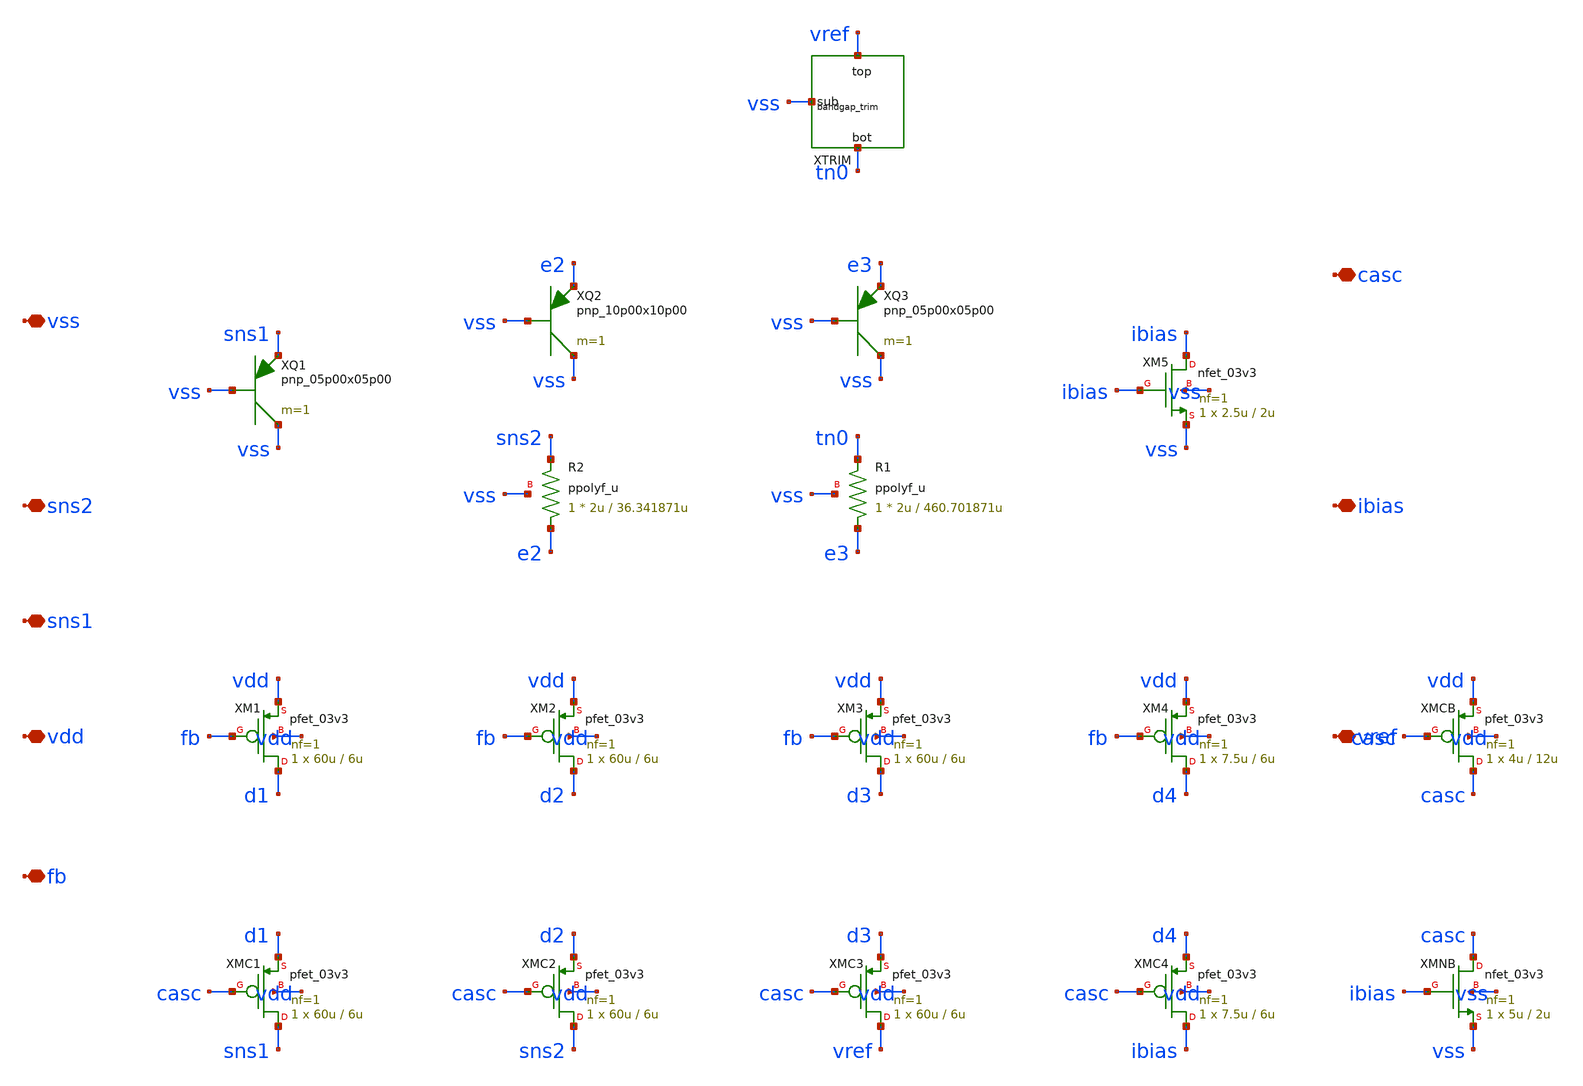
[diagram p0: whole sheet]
** sch_path: design/bandgap_core.sch
**.subckt bandgap_core vdd vss fb sns1 sns2 vref ibias casc
*.iopin vdd
*.iopin vss
*.iopin fb
*.iopin sns1
*.iopin sns2
*.iopin vref
*.iopin ibias
*.iopin casc
XM1 d1 fb vdd vdd pfet_03v3 L=6u W=60u nf=1 ad='int((nf+1)/2) * W/nf * 0.18u' as='int((nf+2)/2) * W/nf * 0.18u'
+ pd='2*int((nf+1)/2) * (W/nf + 0.18u)' ps='2*int((nf+2)/2) * (W/nf + 0.18u)' nrd='0.18u / W' nrs='0.18u / W'
+ sa=0 sb=0 sd=0 m=1
XMC1 sns1 casc d1 vdd pfet_03v3 L=6u W=60u nf=1 ad='int((nf+1)/2) * W/nf * 0.18u' as='int((nf+2)/2) * W/nf * 0.18u'
+ pd='2*int((nf+1)/2) * (W/nf + 0.18u)' ps='2*int((nf+2)/2) * (W/nf + 0.18u)' nrd='0.18u / W' nrs='0.18u / W'
+ sa=0 sb=0 sd=0 m=1
XQ1 vss vss sns1 pnp_05p00x05p00 m=1 par=1
XM2 d2 fb vdd vdd pfet_03v3 L=6u W=60u nf=1 ad='int((nf+1)/2) * W/nf * 0.18u' as='int((nf+2)/2) * W/nf * 0.18u'
+ pd='2*int((nf+1)/2) * (W/nf + 0.18u)' ps='2*int((nf+2)/2) * (W/nf + 0.18u)' nrd='0.18u / W' nrs='0.18u / W'
+ sa=0 sb=0 sd=0 m=1
XMC2 sns2 casc d2 vdd pfet_03v3 L=6u W=60u nf=1 ad='int((nf+1)/2) * W/nf * 0.18u' as='int((nf+2)/2) * W/nf * 0.18u'
+ pd='2*int((nf+1)/2) * (W/nf + 0.18u)' ps='2*int((nf+2)/2) * (W/nf + 0.18u)' nrd='0.18u / W' nrs='0.18u / W'
+ sa=0 sb=0 sd=0 m=1
XR2 e2 sns2 vss ppolyf_u r_width=2u r_length=36.341871u m=1
XQ2 vss vss e2 pnp_10p00x10p00 m=1
XM3 d3 fb vdd vdd pfet_03v3 L=6u W=60u nf=1 ad='int((nf+1)/2) * W/nf * 0.18u' as='int((nf+2)/2) * W/nf * 0.18u'
+ pd='2*int((nf+1)/2) * (W/nf + 0.18u)' ps='2*int((nf+2)/2) * (W/nf + 0.18u)' nrd='0.18u / W' nrs='0.18u / W'
+ sa=0 sb=0 sd=0 m=1
XMC3 vref casc d3 vdd pfet_03v3 L=6u W=60u nf=1 ad='int((nf+1)/2) * W/nf * 0.18u' as='int((nf+2)/2) * W/nf * 0.18u'
+ pd='2*int((nf+1)/2) * (W/nf + 0.18u)' ps='2*int((nf+2)/2) * (W/nf + 0.18u)' nrd='0.18u / W' nrs='0.18u / W'
+ sa=0 sb=0 sd=0 m=1
XR1 e3 tn0 vss ppolyf_u r_width=2u r_length=460.701871u m=1
XQ3 vss vss e3 pnp_05p00x05p00 m=1 par=1
XM4 d4 fb vdd vdd pfet_03v3 L=6u W=7.5u nf=1 ad='int((nf+1)/2) * W/nf * 0.18u' as='int((nf+2)/2) * W/nf * 0.18u'
+ pd='2*int((nf+1)/2) * (W/nf + 0.18u)' ps='2*int((nf+2)/2) * (W/nf + 0.18u)' nrd='0.18u / W' nrs='0.18u / W'
+ sa=0 sb=0 sd=0 m=1
XMC4 ibias casc d4 vdd pfet_03v3 L=6u W=7.5u nf=1 ad='int((nf+1)/2) * W/nf * 0.18u' as='int((nf+2)/2) * W/nf * 0.18u'
+ pd='2*int((nf+1)/2) * (W/nf + 0.18u)' ps='2*int((nf+2)/2) * (W/nf + 0.18u)' nrd='0.18u / W' nrs='0.18u / W'
+ sa=0 sb=0 sd=0 m=1
XM5 ibias ibias vss vss nfet_03v3 L=2u W=2.5u nf=1 ad='int((nf+1)/2) * W/nf * 0.18u' as='int((nf+2)/2) * W/nf * 0.18u'
+ pd='2*int((nf+1)/2) * (W/nf + 0.18u)' ps='2*int((nf+2)/2) * (W/nf + 0.18u)' nrd='0.18u / W' nrs='0.18u / W'
+ sa=0 sb=0 sd=0 m=1
XMCB casc casc vdd vdd pfet_03v3 L=12u W=4u nf=1 ad='int((nf+1)/2) * W/nf * 0.18u' as='int((nf+2)/2) * W/nf * 0.18u'
+ pd='2*int((nf+1)/2) * (W/nf + 0.18u)' ps='2*int((nf+2)/2) * (W/nf + 0.18u)' nrd='0.18u / W' nrs='0.18u / W'
+ sa=0 sb=0 sd=0 m=1
XMNB casc ibias vss vss nfet_03v3 L=2u W=5u nf=1 ad='int((nf+1)/2) * W/nf * 0.18u' as='int((nf+2)/2) * W/nf * 0.18u'
+ pd='2*int((nf+1)/2) * (W/nf + 0.18u)' ps='2*int((nf+2)/2) * (W/nf + 0.18u)' nrd='0.18u / W' nrs='0.18u / W'
+ sa=0 sb=0 sd=0 m=1
XXTRIM tn0 vref vss bandgap_trim
**.ends

* expanding   symbol:  bandgap_trim.sym # of pins=3
** sym_path: design/bandgap_trim.sym
** sch_path: design/bandgap_trim.sch
.subckt bandgap_trim bot top sub

*.iopin bot
*.iopin top
*.iopin sub
**** begin user architecture code

.param trim_code=32

**** end user architecture code
XRU0 bot tn1 sub ppolyf_u r_width=2u r_length=2.771871u m=1
RS0 tn1 bot {1e-3 + 1e12*(floor(trim_code/1)-2*floor(trim_code/2))} m=1
XRU1 tn1 u1_0 sub ppolyf_u r_width=2u r_length=2.771871u m=1
XRU2 u1_0 tn2 sub ppolyf_u r_width=2u r_length=2.771871u m=1
RS1 tn2 tn1 {1e-3 + 1e12*(floor(trim_code/2)-2*floor(trim_code/4))} m=1
XRU3 tn2 u2_0 sub ppolyf_u r_width=2u r_length=2.771871u m=1
XRU4 u2_0 u2_1 sub ppolyf_u r_width=2u r_length=2.771871u m=1
XRU5 u2_1 u2_2 sub ppolyf_u r_width=2u r_length=2.771871u m=1
XRU6 u2_2 tn3 sub ppolyf_u r_width=2u r_length=2.771871u m=1
RS2 tn3 tn2 {1e-3 + 1e12*(floor(trim_code/4)-2*floor(trim_code/8))} m=1
XRU7 tn3 u3_0 sub ppolyf_u r_width=2u r_length=2.771871u m=1
XRU8 u3_0 u3_1 sub ppolyf_u r_width=2u r_length=2.771871u m=1
XRU9 u3_1 u3_2 sub ppolyf_u r_width=2u r_length=2.771871u m=1
XRU10 u3_2 u3_3 sub ppolyf_u r_width=2u r_length=2.771871u m=1
XRU11 u3_3 u3_4 sub ppolyf_u r_width=2u r_length=2.771871u m=1
XRU12 u3_4 u3_5 sub ppolyf_u r_width=2u r_length=2.771871u m=1
XRU13 u3_5 u3_6 sub ppolyf_u r_width=2u r_length=2.771871u m=1
XRU14 u3_6 tn4 sub ppolyf_u r_width=2u r_length=2.771871u m=1
RS3 tn4 tn3 {1e-3 + 1e12*(floor(trim_code/8)-2*floor(trim_code/16))} m=1
XRU15 tn4 u4_0 sub ppolyf_u r_width=2u r_length=2.771871u m=1
XRU16 u4_0 u4_1 sub ppolyf_u r_width=2u r_length=2.771871u m=1
XRU17 u4_1 u4_2 sub ppolyf_u r_width=2u r_length=2.771871u m=1
XRU18 u4_2 u4_3 sub ppolyf_u r_width=2u r_length=2.771871u m=1
XRU19 u4_3 u4_4 sub ppolyf_u r_width=2u r_length=2.771871u m=1
XRU20 u4_4 u4_5 sub ppolyf_u r_width=2u r_length=2.771871u m=1
XRU21 u4_5 u4_6 sub ppolyf_u r_width=2u r_length=2.771871u m=1
XRU22 u4_6 u4_7 sub ppolyf_u r_width=2u r_length=2.771871u m=1
XRU23 u4_7 u4_8 sub ppolyf_u r_width=2u r_length=2.771871u m=1
XRU24 u4_8 u4_9 sub ppolyf_u r_width=2u r_length=2.771871u m=1
XRU25 u4_9 u4_10 sub ppolyf_u r_width=2u r_length=2.771871u m=1
XRU26 u4_10 u4_11 sub ppolyf_u r_width=2u r_length=2.771871u m=1
XRU27 u4_11 u4_12 sub ppolyf_u r_width=2u r_length=2.771871u m=1
XRU28 u4_12 u4_13 sub ppolyf_u r_width=2u r_length=2.771871u m=1
XRU29 u4_13 u4_14 sub ppolyf_u r_width=2u r_length=2.771871u m=1
XRU30 u4_14 tn5 sub ppolyf_u r_width=2u r_length=2.771871u m=1
RS4 tn5 tn4 {1e-3 + 1e12*(floor(trim_code/16)-2*floor(trim_code/32))} m=1
XRU31 tn5 u5_0 sub ppolyf_u r_width=2u r_length=2.771871u m=1
XRU32 u5_0 u5_1 sub ppolyf_u r_width=2u r_length=2.771871u m=1
XRU33 u5_1 u5_2 sub ppolyf_u r_width=2u r_length=2.771871u m=1
XRU34 u5_2 u5_3 sub ppolyf_u r_width=2u r_length=2.771871u m=1
XRU35 u5_3 u5_4 sub ppolyf_u r_width=2u r_length=2.771871u m=1
XRU36 u5_4 u5_5 sub ppolyf_u r_width=2u r_length=2.771871u m=1
XRU37 u5_5 u5_6 sub ppolyf_u r_width=2u r_length=2.771871u m=1
XRU38 u5_6 u5_7 sub ppolyf_u r_width=2u r_length=2.771871u m=1
XRU39 u5_7 u5_8 sub ppolyf_u r_width=2u r_length=2.771871u m=1
XRU40 u5_8 u5_9 sub ppolyf_u r_width=2u r_length=2.771871u m=1
XRU41 u5_9 u5_10 sub ppolyf_u r_width=2u r_length=2.771871u m=1
XRU42 u5_10 u5_11 sub ppolyf_u r_width=2u r_length=2.771871u m=1
XRU43 u5_11 u5_12 sub ppolyf_u r_width=2u r_length=2.771871u m=1
XRU44 u5_12 u5_13 sub ppolyf_u r_width=2u r_length=2.771871u m=1
XRU45 u5_13 u5_14 sub ppolyf_u r_width=2u r_length=2.771871u m=1
XRU46 u5_14 u5_15 sub ppolyf_u r_width=2u r_length=2.771871u m=1
XRU47 u5_15 u5_16 sub ppolyf_u r_width=2u r_length=2.771871u m=1
XRU48 u5_16 u5_17 sub ppolyf_u r_width=2u r_length=2.771871u m=1
XRU49 u5_17 u5_18 sub ppolyf_u r_width=2u r_length=2.771871u m=1
XRU50 u5_18 u5_19 sub ppolyf_u r_width=2u r_length=2.771871u m=1
XRU51 u5_19 u5_20 sub ppolyf_u r_width=2u r_length=2.771871u m=1
XRU52 u5_20 u5_21 sub ppolyf_u r_width=2u r_length=2.771871u m=1
XRU53 u5_21 u5_22 sub ppolyf_u r_width=2u r_length=2.771871u m=1
XRU54 u5_22 u5_23 sub ppolyf_u r_width=2u r_length=2.771871u m=1
XRU55 u5_23 u5_24 sub ppolyf_u r_width=2u r_length=2.771871u m=1
XRU56 u5_24 u5_25 sub ppolyf_u r_width=2u r_length=2.771871u m=1
XRU57 u5_25 u5_26 sub ppolyf_u r_width=2u r_length=2.771871u m=1
XRU58 u5_26 u5_27 sub ppolyf_u r_width=2u r_length=2.771871u m=1
XRU59 u5_27 u5_28 sub ppolyf_u r_width=2u r_length=2.771871u m=1
XRU60 u5_28 u5_29 sub ppolyf_u r_width=2u r_length=2.771871u m=1
XRU61 u5_29 u5_30 sub ppolyf_u r_width=2u r_length=2.771871u m=1
XRU62 u5_30 top sub ppolyf_u r_width=2u r_length=2.771871u m=1
RS5 top tn5 {1e-3 + 1e12*(floor(trim_code/32)-2*floor(trim_code/64))} m=1
.ends

.end
